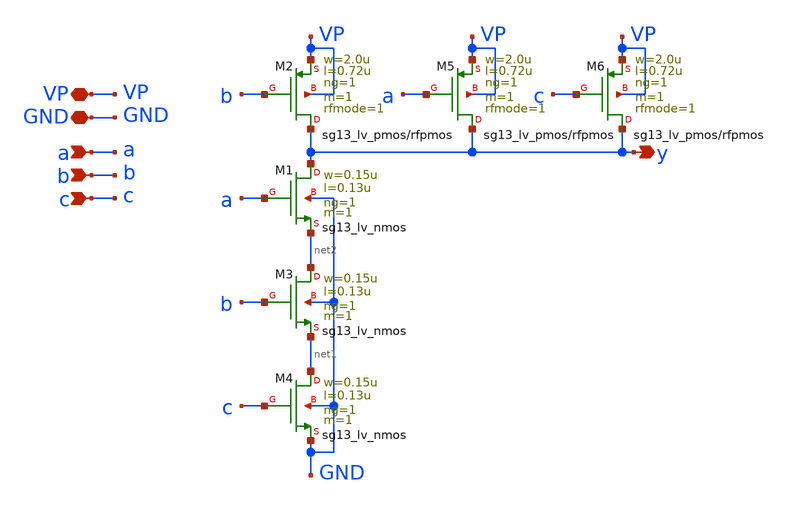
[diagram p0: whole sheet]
** sch_path: schematics/divider/NAND_3in.sch
**.subckt NAND_3in y GND a VP b c
*.opin y
*.iopin GND
*.ipin a
*.iopin VP
*.ipin b
*.ipin c
XM1 y a net2 GND sg13_lv_nmos w=0.15u l=0.13u ng=1 m=1 mm_ok=1
XM2 y b VP VP sg13_lv_pmos w=2.0u l=0.72u ng=1 m=1 rfmode=1 mm_ok=1
XM3 net2 b net1 GND sg13_lv_nmos w=0.15u l=0.13u ng=1 m=1 mm_ok=1
XM4 net1 c GND GND sg13_lv_nmos w=0.15u l=0.13u ng=1 m=1 mm_ok=1
XM5 y a VP VP sg13_lv_pmos w=2.0u l=0.72u ng=1 m=1 rfmode=1 mm_ok=1
XM6 y c VP VP sg13_lv_pmos w=2.0u l=0.72u ng=1 m=1 rfmode=1 mm_ok=1
**.ends
.end
